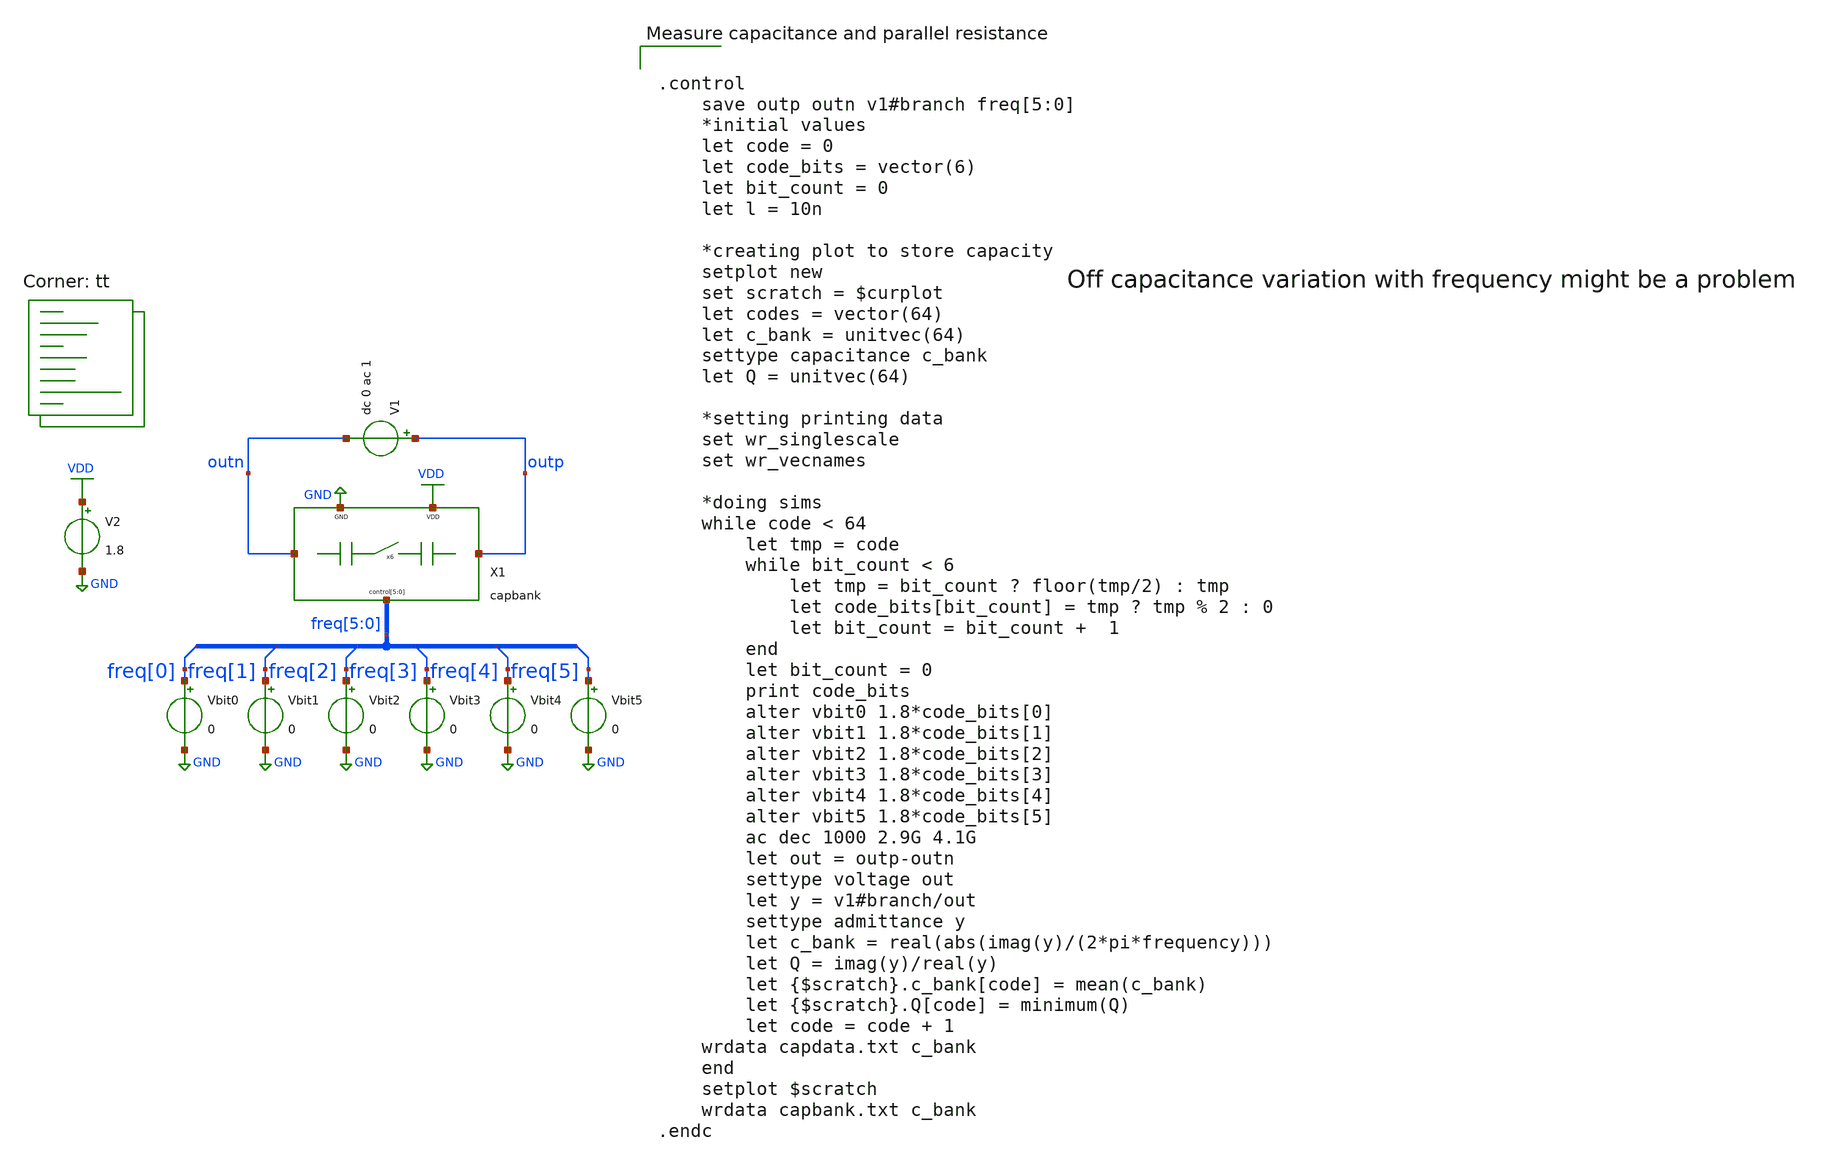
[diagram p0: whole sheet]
** sch_path: xschem/vco/testbenches/capbank/capbank_capacity_measurement_tb.sch
**.subckt capbank_capacity_measurement_tb
X1 outn outp VDD freq[5] freq[4] freq[3] freq[2] freq[1] freq[0] GND capbank
Vbit0 freq[0] GND 0
Vbit1 freq[1] GND 0
Vbit2 freq[2] GND 0
Vbit3 freq[3] GND 0
Vbit4 freq[4] GND 0
Vbit5 freq[5] GND 0
V1 outp outn dc 0 ac 1
V2 VDD GND 1.8
**** begin user architecture code
.lib $::SKYWATER_MODELS/sky130.lib.spice tt


.control
    save outp outn v1#branch freq[5:0]
    *initial values
    let code = 0
    let code_bits = vector(6)
    let bit_count = 0
    let l = 10n

    *creating plot to store capacity
    setplot new
    set scratch = $curplot
    let codes = vector(64)
    let c_bank = unitvec(64)
    settype capacitance c_bank
    let Q = unitvec(64)

    *setting printing data
    set wr_singlescale
    set wr_vecnames

    *doing sims
    while code < 64
        let tmp = code
        while bit_count < 6
            let tmp = bit_count ? floor(tmp/2) : tmp
            let code_bits[bit_count] = tmp ? tmp % 2 : 0
            let bit_count = bit_count +  1
        end
        let bit_count = 0
        print code_bits
        alter vbit0 1.8*code_bits[0]
        alter vbit1 1.8*code_bits[1]
        alter vbit2 1.8*code_bits[2]
        alter vbit3 1.8*code_bits[3]
        alter vbit4 1.8*code_bits[4]
        alter vbit5 1.8*code_bits[5]
        ac dec 1000 2.9G 4.1G
        let out = outp-outn
        settype voltage out
        let y = v1#branch/out
        settype admittance y
        let c_bank = real(abs(imag(y)/(2*pi*frequency)))
        let Q = imag(y)/real(y)
        let {$scratch}.c_bank[code] = mean(c_bank)
        let {$scratch}.Q[code] = minimum(Q)
        let code = code + 1
	wrdata capdata.txt c_bank
    end
    setplot $scratch
    wrdata capbank.txt c_bank
.endc


**** end user architecture code
**.ends
.GLOBAL VDD
.GLOBAL GND
.end
